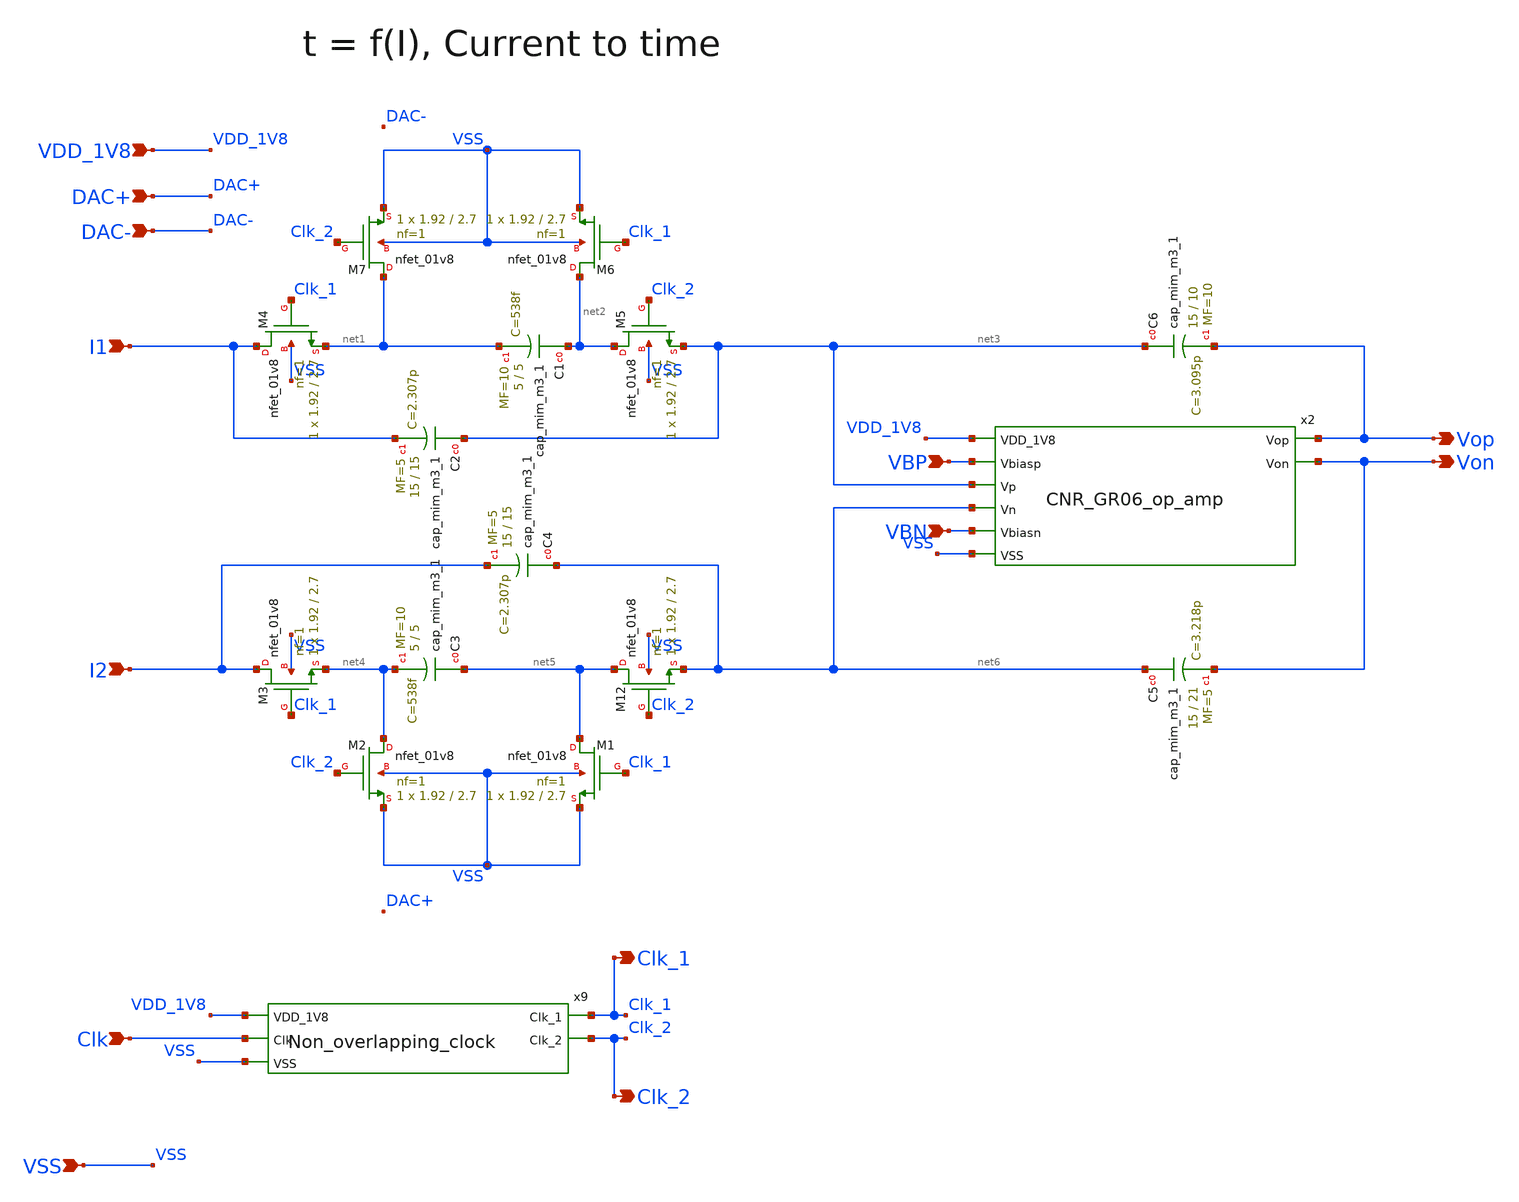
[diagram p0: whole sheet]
** sch_path: design/CNR_GR06_SKY130NM/CNR_GR06_I_to_t.sch
**.subckt CNR_GR06_I_to_t I2 VDD_1V8 VSS I1 Clk Von Vop Clk_1 Clk_2 DAC+ DAC- VBN VBP
*.ipin I2
*.ipin VDD_1V8
*.ipin VSS
*.ipin I1
*.ipin Clk
*.opin Von
*.opin Vop
*.opin Clk_1
*.opin Clk_2
*.ipin DAC+
*.ipin DAC-
*.ipin VBN
*.ipin VBP
XC1 net2 net1 sky130_fd_pr__cap_mim_m3_1 W=5 L=5 MF=10 m=10
XC2 net3 I1 sky130_fd_pr__cap_mim_m3_1 W=15 L=15 MF=5 m=5
XC3 net5 net4 sky130_fd_pr__cap_mim_m3_1 W=5 L=5 MF=10 m=10
XC4 net6 I2 sky130_fd_pr__cap_mim_m3_1 W=15 L=15 MF=5 m=5
XC5 net6 Von sky130_fd_pr__cap_mim_m3_1 W=15 L=21 MF=5 m=5
XC6 net3 Vop sky130_fd_pr__cap_mim_m3_1 W=15 L=10 MF=10 m=10
x9 VDD_1V8 Clk Clk_1 Clk_2 VSS Non_overlapping_clock
x2 VDD_1V8 VBP Vop net3 Von net6 VBN VSS CNR_GR06_op_amp
XM12 net5 Clk_2 net6 VSS sky130_fd_pr__nfet_01v8 L=2.7 W=1.92 nf=1 ad='int((nf+1)/2) * W/nf * 0.29' as='int((nf+2)/2) * W/nf * 0.29'
+ pd='2*int((nf+1)/2) * (W/nf + 0.29)' ps='2*int((nf+2)/2) * (W/nf + 0.29)' nrd='0.29 / W' nrs='0.29 / W'
+ sa=0 sb=0 sd=0 mult=1 m=1
XM1 net5 Clk_1 VSS VSS sky130_fd_pr__nfet_01v8 L=2.7 W=1.92 nf=1 ad='int((nf+1)/2) * W/nf * 0.29' as='int((nf+2)/2) * W/nf * 0.29'
+ pd='2*int((nf+1)/2) * (W/nf + 0.29)' ps='2*int((nf+2)/2) * (W/nf + 0.29)' nrd='0.29 / W' nrs='0.29 / W'
+ sa=0 sb=0 sd=0 mult=1 m=1
XM2 net4 Clk_2 VSS VSS sky130_fd_pr__nfet_01v8 L=2.7 W=1.92 nf=1 ad='int((nf+1)/2) * W/nf * 0.29' as='int((nf+2)/2) * W/nf * 0.29'
+ pd='2*int((nf+1)/2) * (W/nf + 0.29)' ps='2*int((nf+2)/2) * (W/nf + 0.29)' nrd='0.29 / W' nrs='0.29 / W'
+ sa=0 sb=0 sd=0 mult=1 m=1
XM3 I2 Clk_1 net4 VSS sky130_fd_pr__nfet_01v8 L=2.7 W=1.92 nf=1 ad='int((nf+1)/2) * W/nf * 0.29' as='int((nf+2)/2) * W/nf * 0.29'
+ pd='2*int((nf+1)/2) * (W/nf + 0.29)' ps='2*int((nf+2)/2) * (W/nf + 0.29)' nrd='0.29 / W' nrs='0.29 / W'
+ sa=0 sb=0 sd=0 mult=1 m=1
XM4 I1 Clk_1 net1 VSS sky130_fd_pr__nfet_01v8 L=2.7 W=1.92 nf=1 ad='int((nf+1)/2) * W/nf * 0.29' as='int((nf+2)/2) * W/nf * 0.29'
+ pd='2*int((nf+1)/2) * (W/nf + 0.29)' ps='2*int((nf+2)/2) * (W/nf + 0.29)' nrd='0.29 / W' nrs='0.29 / W'
+ sa=0 sb=0 sd=0 mult=1 m=1
XM5 net2 Clk_2 net3 VSS sky130_fd_pr__nfet_01v8 L=2.7 W=1.92 nf=1 ad='int((nf+1)/2) * W/nf * 0.29' as='int((nf+2)/2) * W/nf * 0.29'
+ pd='2*int((nf+1)/2) * (W/nf + 0.29)' ps='2*int((nf+2)/2) * (W/nf + 0.29)' nrd='0.29 / W' nrs='0.29 / W'
+ sa=0 sb=0 sd=0 mult=1 m=1
XM6 net2 Clk_1 VSS VSS sky130_fd_pr__nfet_01v8 L=2.7 W=1.92 nf=1 ad='int((nf+1)/2) * W/nf * 0.29' as='int((nf+2)/2) * W/nf * 0.29'
+ pd='2*int((nf+1)/2) * (W/nf + 0.29)' ps='2*int((nf+2)/2) * (W/nf + 0.29)' nrd='0.29 / W' nrs='0.29 / W'
+ sa=0 sb=0 sd=0 mult=1 m=1
XM7 net1 Clk_2 VSS VSS sky130_fd_pr__nfet_01v8 L=2.7 W=1.92 nf=1 ad='int((nf+1)/2) * W/nf * 0.29' as='int((nf+2)/2) * W/nf * 0.29'
+ pd='2*int((nf+1)/2) * (W/nf + 0.29)' ps='2*int((nf+2)/2) * (W/nf + 0.29)' nrd='0.29 / W' nrs='0.29 / W'
+ sa=0 sb=0 sd=0 mult=1 m=1
**.ends
.end
